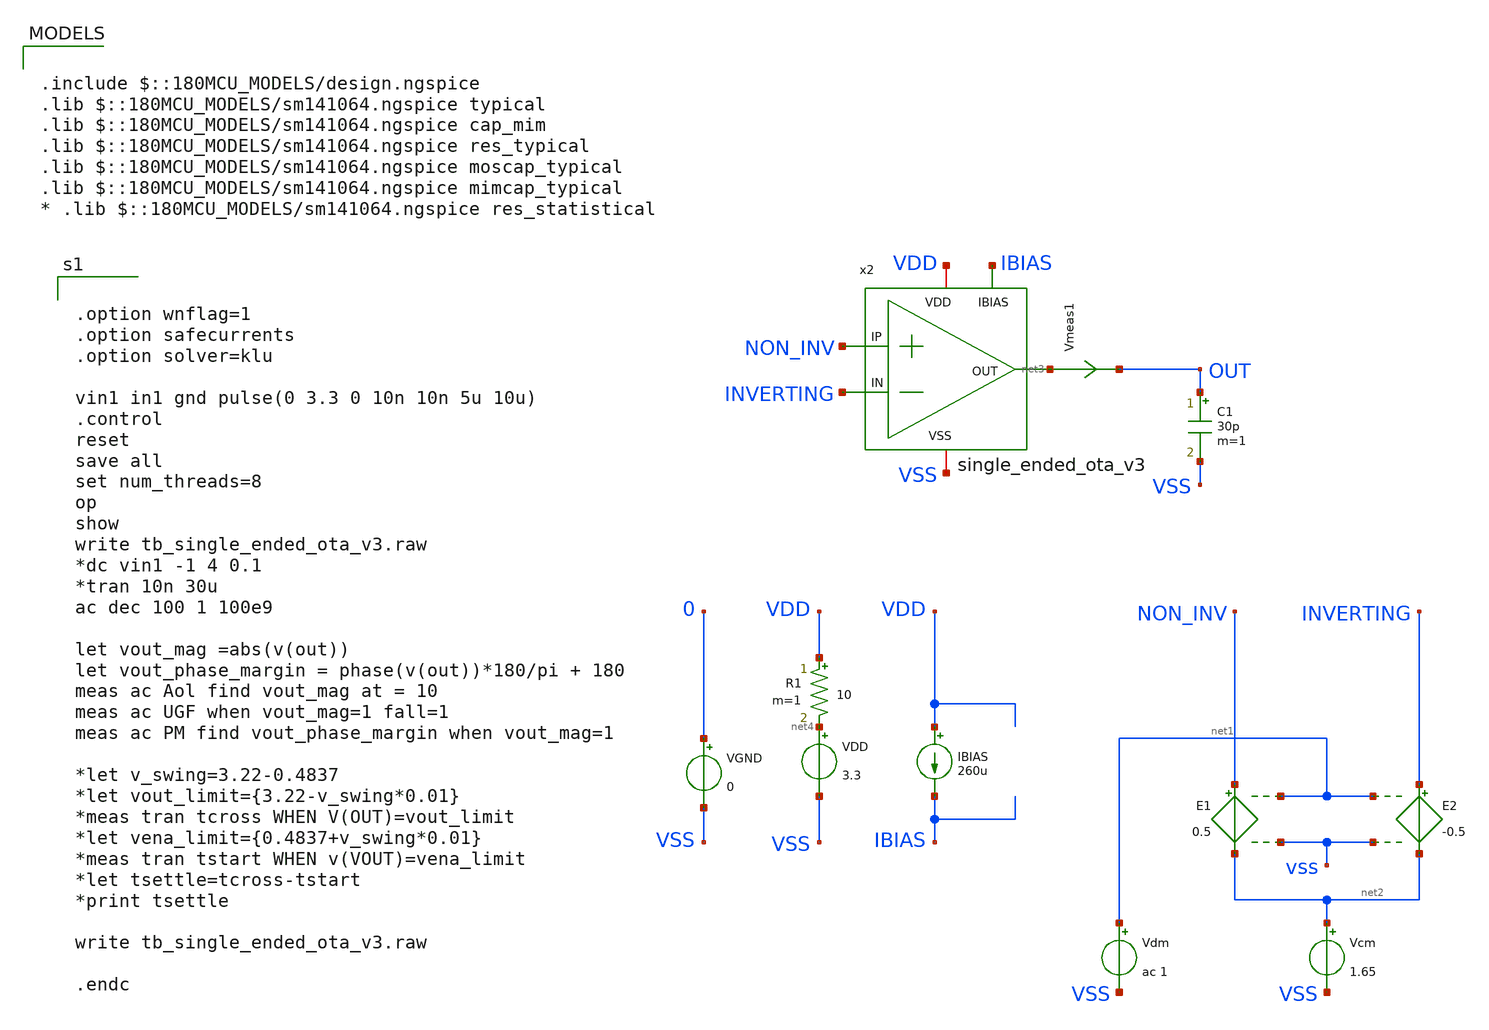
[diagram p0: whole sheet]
** sch_path: designs/libs/tb_ota/tb_three_single_ended_ota/tb_single_ended_ota_v3.sch
**.subckt tb_single_ended_ota_v3
E1 NON_INV net2 net1 vss 0.5
E2 INVERTING net2 net1 vss -0.5
Vdm net1 VSS ac 1
Vcm net2 VSS 1.65
C1 OUT VSS 30p m=1
Vmeas1 net3 OUT 0
.save i(vmeas1)
VDD net4 VSS 3.3
R1 VDD net4 10 m=1
IBIAS VDD IBIAS 260u
VGND 0 VSS 0
x2 NON_INV INVERTING IBIAS net3 VDD VSS single_ended_ota_v3
**** begin user architecture code


.option wnflag=1
.option safecurrents
.option solver=klu

vin1 in1 gnd pulse(0 3.3 0 10n 10n 5u 10u)
.control
reset
save all
set num_threads=8
op
show
write tb_single_ended_ota_v3.raw
*dc vin1 -1 4 0.1
*tran 10n 30u
ac dec 100 1 100e9

let vout_mag =abs(v(out))
let vout_phase_margin = phase(v(out))*180/pi + 180
meas ac Aol find vout_mag at = 10
meas ac UGF when vout_mag=1 fall=1
meas ac PM find vout_phase_margin when vout_mag=1

*let v_swing=3.22-0.4837
*let vout_limit={3.22-v_swing*0.01}
*meas tran tcross WHEN V(OUT)=vout_limit
*let vena_limit={0.4837+v_swing*0.01}
*meas tran tstart WHEN v(VOUT)=vena_limit
*let tsettle=tcross-tstart
*print tsettle

write tb_single_ended_ota_v3.raw

.endc



.include $::180MCU_MODELS/design.ngspice
.lib $::180MCU_MODELS/sm141064.ngspice typical
.lib $::180MCU_MODELS/sm141064.ngspice cap_mim
.lib $::180MCU_MODELS/sm141064.ngspice res_typical
.lib $::180MCU_MODELS/sm141064.ngspice moscap_typical
.lib $::180MCU_MODELS/sm141064.ngspice mimcap_typical
* .lib $::180MCU_MODELS/sm141064.ngspice res_statistical

**** end user architecture code
**.ends
.end
